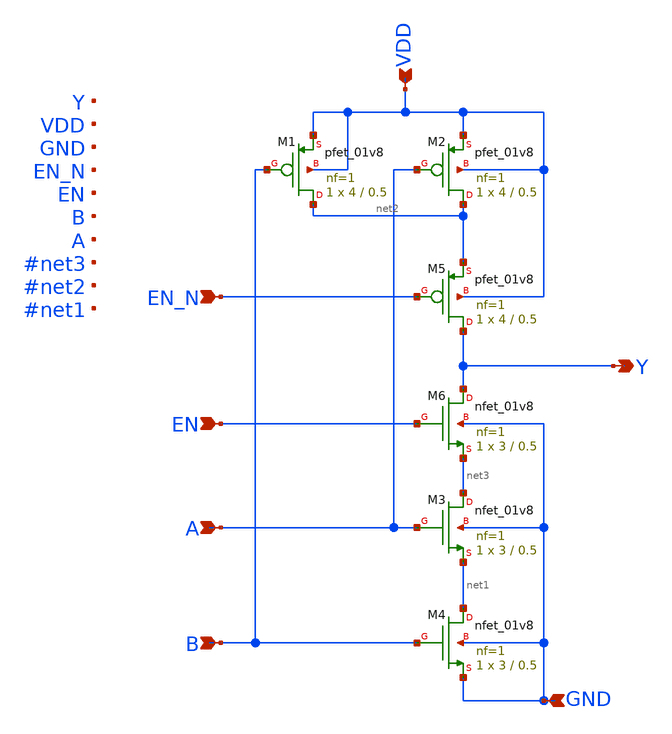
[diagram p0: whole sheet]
** sch_path: ADC/4bit_C2C/MagicAndSpice/EE431_FinalProj/tristate_NAND2.sch
**.subckt tristate_NAND2 A B VDD GND Y EN EN_N
*.ipin A
*.ipin B
*.ipin VDD
*.ipin GND
*.opin Y
*.ipin EN
*.ipin EN_N
XM1 net2 B VDD VDD sky130_fd_pr__pfet_01v8 L=0.5 W=4 nf=1 ad='int((nf+1)/2) * W/nf * 0.29' as='int((nf+2)/2) * W/nf * 0.29'
+ pd='2*int((nf+1)/2) * (W/nf + 0.29)' ps='2*int((nf+2)/2) * (W/nf + 0.29)' nrd='0.29 / W' nrs='0.29 / W'
+ sa=0 sb=0 sd=0 mult=1 m=1
XM2 net2 A VDD VDD sky130_fd_pr__pfet_01v8 L=0.5 W=4 nf=1 ad='int((nf+1)/2) * W/nf * 0.29' as='int((nf+2)/2) * W/nf * 0.29'
+ pd='2*int((nf+1)/2) * (W/nf + 0.29)' ps='2*int((nf+2)/2) * (W/nf + 0.29)' nrd='0.29 / W' nrs='0.29 / W'
+ sa=0 sb=0 sd=0 mult=1 m=1
XM3 net3 A net1 GND sky130_fd_pr__nfet_01v8 L=0.5 W=3 nf=1 ad='int((nf+1)/2) * W/nf * 0.29' as='int((nf+2)/2) * W/nf * 0.29'
+ pd='2*int((nf+1)/2) * (W/nf + 0.29)' ps='2*int((nf+2)/2) * (W/nf + 0.29)' nrd='0.29 / W' nrs='0.29 / W'
+ sa=0 sb=0 sd=0 mult=1 m=1
XM4 net1 B GND GND sky130_fd_pr__nfet_01v8 L=0.5 W=3 nf=1 ad='int((nf+1)/2) * W/nf * 0.29' as='int((nf+2)/2) * W/nf * 0.29'
+ pd='2*int((nf+1)/2) * (W/nf + 0.29)' ps='2*int((nf+2)/2) * (W/nf + 0.29)' nrd='0.29 / W' nrs='0.29 / W'
+ sa=0 sb=0 sd=0 mult=1 m=1
XM5 Y EN_N net2 VDD sky130_fd_pr__pfet_01v8 L=0.5 W=4 nf=1 ad='int((nf+1)/2) * W/nf * 0.29' as='int((nf+2)/2) * W/nf * 0.29'
+ pd='2*int((nf+1)/2) * (W/nf + 0.29)' ps='2*int((nf+2)/2) * (W/nf + 0.29)' nrd='0.29 / W' nrs='0.29 / W'
+ sa=0 sb=0 sd=0 mult=1 m=1
XM6 Y EN net3 GND sky130_fd_pr__nfet_01v8 L=0.5 W=3 nf=1 ad='int((nf+1)/2) * W/nf * 0.29' as='int((nf+2)/2) * W/nf * 0.29'
+ pd='2*int((nf+1)/2) * (W/nf + 0.29)' ps='2*int((nf+2)/2) * (W/nf + 0.29)' nrd='0.29 / W' nrs='0.29 / W'
+ sa=0 sb=0 sd=0 mult=1 m=1
**.ends
.end
